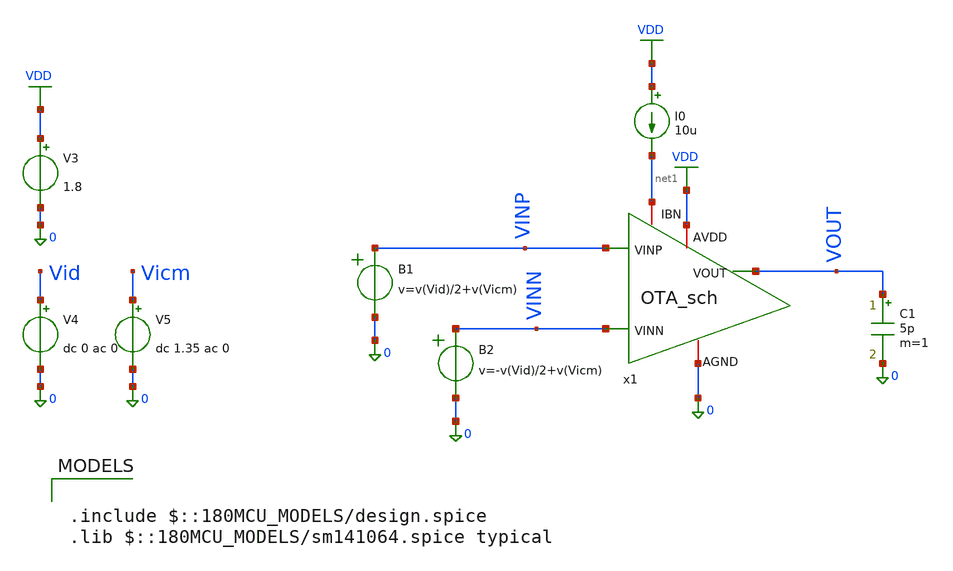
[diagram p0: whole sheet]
** sch_path: Lab_07/OTA_tb.sch
**.subckt OTA_tb
x1 VINP VDD VINN net1 0 VOUT OTA_sch
V3 VDD 0 1.8
V4 Vid 0 dc 0 ac 0
V5 Vicm 0 dc 1.35 ac 0
I0 VDD net1 10u
C1 VOUT 0 5p m=1
B1 VINP 0 v=v(Vid)/2+v(Vicm)
B2 VINN 0 v=-v(Vid)/2+v(Vicm)
**** begin user architecture code

.include $::180MCU_MODELS/design.spice
.lib $::180MCU_MODELS/sm141064.spice typical


.control
alterparam sw_stat_global = 0
alterparam sw_stat_mismatch = 0
reset
save all
let x = 1
set num = {$&x}
dowhile x <= 6
save @m.x1.xm{$num}.m0[id]
save @m.x1.xm{$num}.m0[vgs]
save @m.x1.xm{$num}.m0[vds]
save @m.x1.xm{$num}.m0[vdsat]
save @m.x1.xm{$num}.m0[vth]
save @m.x1.xm{$num}.m0[gm]
save @m.x1.xm{$num}.m0[gds]
save @m.x1.xm{$num}.m0[gmbs]
save @m.x1.xm{$num}.m0[cgg]
save @m.x1.xm{$num}.m0[cdd]
save @m.x1.xm{$num}.m0[css]
save @m.x1.xm{$num}.m0[cgd]
save @m.x1.xm{$num}.m0[cdb]
let x = x + 1
set num = {$&x}
end


* === OP Point ===
op
write 5t_ota_tb_ol.raw
set appendwrite
echo " === MOSFET Operating Points ==="
show m : id : vgs : vds : vth : vdsat : gm : gds : gmbs
echo " === Bias Points ==="
let x = 1
dowhile x <= 6
set num = {$&x}
let gmid = @m.x1.xm{$num}.m0[gm]/@m.x1.xm{$num}.m0[id]
let Vstar = 2/gmid
echo "M{$num}: gm/id = $&gmid S/A, Vstar = $&Vstar V"
let x = x + 1
end
* === DIFFERENTIAL AC ===
alter V4 AC = 1
alter V5 AC = 0
ac dec 10 1 10e9
* === COMMON MODE AC ===
alter V4 AC = 0
alter V5 AC = 1
ac dec 10 1 10e9
* === EXTRACT RESULTS ===
set units=degrees
let vod = ac1.v(VOUT)
let vocm = ac2.v(VOUT)
let CMRR = vdb(vod) - vdb(vocm)
* === MEASUREMENTS ===
meas ac Av_diff_db find vdb(vod) at=1
meas ac Av_diff_mag find vmag(vod) at=1
let A3db = Av_diff_mag/sqrt(2)
meas ac BW_diff when vmag(vod)=A3db fall=1
meas ac UGF when vmag(vod)=1 fall=1
meas ac P_UGF find vp(vod) at=UGF
let GBW = Av_diff_mag * BW_diff
let PM = 180 + P_UGF
meas ac Av_CM_db find vdb(vocm) at=1
meas ac Av_CM_mag find vmag(vocm) at=1
let A3db = Av_CM_mag/sqrt(2)
meas ac BW_CM when vmag(vocm)=A3db fall=1
let CMRR_db = Av_diff_db - Av_CM_db


* === DISPLAY RESULTS ===
echo " === AC Results ==="
echo "Av Diff: $&Av_diff_db dB, BW: $&BW_diff Hz"
echo "UGF: $&UGF Hz"
echo "GBW: $&GBW Hz"
echo "PM: $&PM deg"
echo "Av CM: $&Av_CM_db dB, BW: $&BW_CM Hz"
echo "CMRR: $&CMRR_db dB"
write 5t_ota_tb_ol.raw
.endc

**** end user architecture code
**.ends

* expanding   symbol:  OTA_sch.sym # of pins=6
** sym_path: Lab_07/OTA_sch.sym
** sch_path: Lab_07/OTA_sch.sch
.subckt OTA_sch VINP AVDD VINN IBN AGND VOUT
*.iopin AVDD
*.iopin IBN
*.iopin AGND
*.opin VOUT
*.ipin VINN
*.ipin VINP
XM1 net1 VINP net2 AGND nfet_03v3 L=450n W=8.237u nf=1 ad='int((nf+1)/2) * W/nf * 0.18u' as='int((nf+2)/2) * W/nf * 0.18u'
+ pd='2*int((nf+1)/2) * (W/nf + 0.18u)' ps='2*int((nf+2)/2) * (W/nf + 0.18u)' nrd='0.18u / W' nrs='0.18u / W'
+ sa=0 sb=0 sd=0 m=1
XM2 VOUT VINN net2 AGND nfet_03v3 L=450n W=8.237u nf=1 ad='int((nf+1)/2) * W/nf * 0.18u' as='int((nf+2)/2) * W/nf * 0.18u'
+ pd='2*int((nf+1)/2) * (W/nf + 0.18u)' ps='2*int((nf+2)/2) * (W/nf + 0.18u)' nrd='0.18u / W' nrs='0.18u / W'
+ sa=0 sb=0 sd=0 m=1
XM3 net2 IBN AGND AGND nfet_03v3 L=1u W=4.64*2u nf=1 ad='int((nf+1)/2) * W/nf * 0.18u' as='int((nf+2)/2) * W/nf * 0.18u'
+ pd='2*int((nf+1)/2) * (W/nf + 0.18u)' ps='2*int((nf+2)/2) * (W/nf + 0.18u)' nrd='0.18u / W' nrs='0.18u / W'
+ sa=0 sb=0 sd=0 m=1
XM4 IBN IBN AGND AGND nfet_03v3 L=1u W=4.64u nf=1 ad='int((nf+1)/2) * W/nf * 0.18u' as='int((nf+2)/2) * W/nf * 0.18u'
+ pd='2*int((nf+1)/2) * (W/nf + 0.18u)' ps='2*int((nf+2)/2) * (W/nf + 0.18u)' nrd='0.18u / W' nrs='0.18u / W'
+ sa=0 sb=0 sd=0 m=1
XM5 net1 net1 AVDD AVDD pfet_03v3 L=450n W=7.52u nf=1 ad='int((nf+1)/2) * W/nf * 0.18u' as='int((nf+2)/2) * W/nf * 0.18u'
+ pd='2*int((nf+1)/2) * (W/nf + 0.18u)' ps='2*int((nf+2)/2) * (W/nf + 0.18u)' nrd='0.18u / W' nrs='0.18u / W'
+ sa=0 sb=0 sd=0 m=1
XM6 VOUT net1 AVDD AVDD pfet_03v3 L=450n W=7.52u nf=1 ad='int((nf+1)/2) * W/nf * 0.18u' as='int((nf+2)/2) * W/nf * 0.18u'
+ pd='2*int((nf+1)/2) * (W/nf + 0.18u)' ps='2*int((nf+2)/2) * (W/nf + 0.18u)' nrd='0.18u / W' nrs='0.18u / W'
+ sa=0 sb=0 sd=0 m=1
.ends

.GLOBAL VDD
.end
